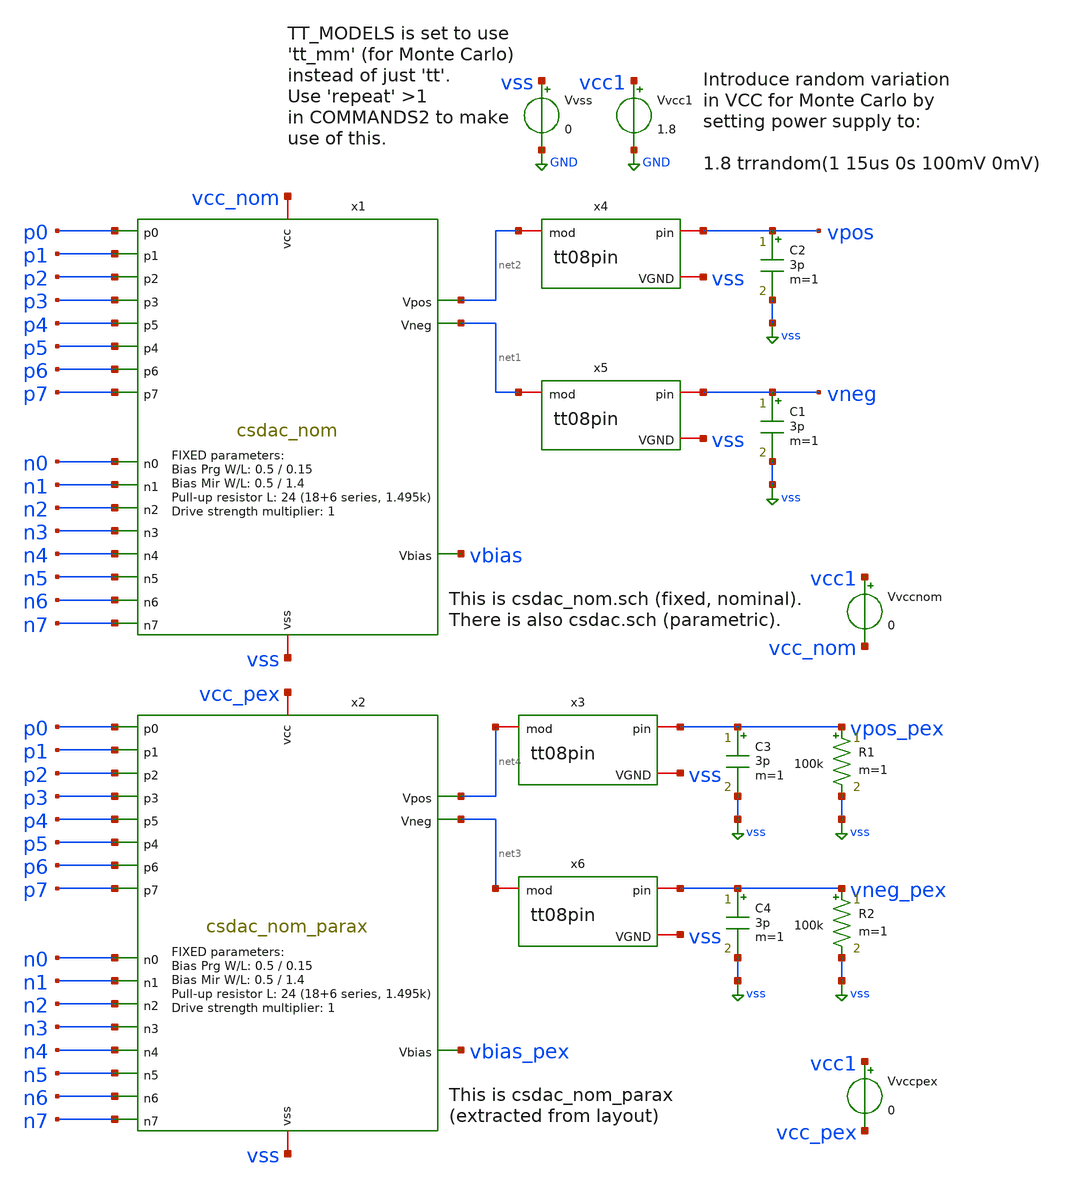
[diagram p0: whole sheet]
** sch_path: xschem/tb_csdac_nom.sch
**.subckt tb_csdac_nom
Vvcc1 vcc1 GND 1.8
Vvss vss GND 0
x1 vcc_nom vss p0 p1 p2 p3 p4 p5 p6 p7 n0 n1 n2 n3 n4 n5 n6 n7 net2 net1 vbias csdac_nom
x4 vpos net2 vss tt08pin
x5 vneg net1 vss tt08pin
C2 vpos vss 3p m=1
C1 vneg vss 3p m=1
x2 vcc_pex vss p0 p1 p2 p3 p4 p5 p6 p7 n0 n1 n2 n3 n4 n5 n6 n7 net4 net3 vbias_pex csdac_nom_parax
x3 vpos_pex net4 vss tt08pin
x6 vneg_pex net3 vss tt08pin
C3 vpos_pex vss 3p m=1
C4 vneg_pex vss 3p m=1
Vvccnom vcc1 vcc_nom 0
Vvccpex vcc1 vcc_pex 0
R1 vpos_pex vss 100k m=1
R2 vneg_pex vss 100k m=1
**** begin user architecture code



.param singlebits=0
.IF (singlebits == 1)
* Mode to just test each binary-weighted level:
Vxp0 p0 GND pulse 0v 1.8v 1u 1n 1n 1u 10u
Vxp1 p1 GND pulse 0v 1.8v 2u 1n 1n 1u 10u
Vxp2 p2 GND pulse 0v 1.8v 3u 1n 1n 1u 10u
Vxp3 p3 GND pulse 0v 1.8v 4u 1n 1n 1u 10u
Vxp4 p4 GND pulse 0v 1.8v 5u 1n 1n 1u 10u
Vxp5 p5 GND pulse 0v 1.8v 6u 1n 1n 1u 10u
Vxp6 p6 GND pulse 0v 1.8v 7u 1n 1n 1u 10u
Vxp7 p7 GND pulse 0v 1.8v 8u 1n 1n 1u 10u
Vxn0 n0 GND pulse 1.8v 0v 1u 1n 1n 1u 10u
Vxn1 n1 GND pulse 1.8v 0v 2u 1n 1n 1u 10u
Vxn2 n2 GND pulse 1.8v 0v 3u 1n 1n 1u 10u
Vxn3 n3 GND pulse 1.8v 0v 4u 1n 1n 1u 10u
Vxn4 n4 GND pulse 1.8v 0v 5u 1n 1n 1u 10u
Vxn5 n5 GND pulse 1.8v 0v 6u 1n 1n 1u 10u
Vxn6 n6 GND pulse 1.8v 0v 7u 1n 1n 1u 10u
Vxn7 n7 GND pulse 1.8v 0v 8u 1n 1n 1u 10u
.ELSEIF (singlebits == 0)
* Mode to test full 0..255 trange:
Vxp0 p0 GND pulse 1.8v 0v 0n 1n 1n 39n 80n
Vxp1 p1 GND pulse 1.8v 0v 0n 1n 1n 79n 160n
Vxp2 p2 GND pulse 1.8v 0v 0n 1n 1n 159n 320n
Vxp3 p3 GND pulse 1.8v 0v 0n 1n 1n 319n 640n
Vxp4 p4 GND pulse 1.8v 0v 0n 1n 1n 639n 1280n
Vxp5 p5 GND pulse 1.8v 0v 0n 1n 1n 1279n 2560n
Vxp6 p6 GND pulse 1.8v 0v 0n 1n 1n 2559n 5120n
Vxp7 p7 GND pulse 1.8v 0v 0n 1n 1n 5119n 10240n
Vxn0 n0 GND pulse 0v 1.8v 0n 1n 1n 39n 80n
Vxn1 n1 GND pulse 0v 1.8v 0n 1n 1n 79n 160n
Vxn2 n2 GND pulse 0v 1.8v 0n 1n 1n 159n 320n
Vxn3 n3 GND pulse 0v 1.8v 0n 1n 1n 319n 640n
Vxn4 n4 GND pulse 0v 1.8v 0n 1n 1n 639n 1280n
Vxn5 n5 GND pulse 0v 1.8v 0n 1n 1n 1279n 2560n
Vxn6 n6 GND pulse 0v 1.8v 0n 1n 1n 2559n 5120n
Vxn7 n7 GND pulse 0v 1.8v 0n 1n 1n 5119n 10240n
.ENDIF

.options savecurrents
.control

  * If using Monte Carlo, change to repeat to (say) 5:
  repeat 1
    save all
    tran 1n 12.8u
    write tb_csdac.raw i(vvss) vcc1
    + i(vvccnom) vpos     vneg     vbias
    + i(vvccpex) vpos_pex vneg_pex vbias_pex
    set appendwrite
    reset
  end

*  save all
*  *reset
*  *alterparam MPW=4
*  *alterparam MMW=4
*  tran 1n 12.8u
*  write 11.raw i(vvcc) i(vvss) vpos vneg vbias

*  set appendwrite
*  alterparam MPW=4
*  alterparam MMW=4
*  reset
*  tran 1n 12.8u
*  write 11.raw i(vvcc) i(vvss) vpos vneg vbias

.endc




** opencircuitdesign pdks install
.lib $::SKYWATER_MODELS/sky130.lib.spice tt


**** end user architecture code
**.ends

* expanding   symbol:  csdac_nom.sym # of pins=21
** sym_path: xschem/csdac_nom.sym
** sch_path: xschem/csdac_nom.sch
.subckt csdac_nom vcc vss p0 p1 p2 p3 p4 p5 p6 p7 n0 n1 n2 n3 n4 n5 n6 n7 Vpos Vneg Vbias
*.iopin vcc
*.iopin vss
*.ipin p0
*.ipin n0
*.ipin p1
*.ipin n1
*.ipin p2
*.ipin n2
*.ipin p3
*.ipin n3
*.ipin p4
*.ipin n4
*.ipin p5
*.ipin n5
*.ipin p6
*.ipin n6
*.ipin p7
*.ipin n7
*.opin Vpos
*.opin Vneg
*.opin Vbias
XMprog Vbias vss vcc vcc sky130_fd_pr__pfet_01v8 L=0.15 W=0.5 nf=1 ad='int((nf+1)/2) * W/nf * 0.29' as='int((nf+2)/2) * W/nf * 0.29'
+ pd='2*int((nf+1)/2) * (W/nf + 0.29)' ps='2*int((nf+2)/2) * (W/nf + 0.29)' nrd='0.29 / W' nrs='0.29 / W'
+ sa=0 sb=0 sd=0 mult=1 m=1
XMmirror Vbias Vbias vss vss sky130_fd_pr__nfet_01v8 L=0.5 W=0.5 nf=1 ad='int((nf+1)/2) * W/nf * 0.29'
+ as='int((nf+2)/2) * W/nf * 0.29' pd='2*int((nf+1)/2) * (W/nf + 0.29)' ps='2*int((nf+2)/2) * (W/nf + 0.29)'
+ nrd='0.29 / W' nrs='0.29 / W' sa=0 sb=0 sd=0 mult=1 m=1
XMB0 IS0 Vbias vss vss sky130_fd_pr__nfet_01v8 L=16 W=0.5 nf=1 ad='int((nf+1)/2) * W/nf * 0.29' as='int((nf+2)/2) * W/nf * 0.29'
+ pd='2*int((nf+1)/2) * (W/nf + 0.29)' ps='2*int((nf+2)/2) * (W/nf + 0.29)' nrd='0.29 / W' nrs='0.29 / W'
+ sa=0 sb=0 sd=0 mult=1 m=1
XMP0 Vpos p0 IS0 vss sky130_fd_pr__nfet_01v8 L=0.15 W=0.5 nf=1 ad='int((nf+1)/2) * W/nf * 0.29' as='int((nf+2)/2) * W/nf * 0.29'
+ pd='2*int((nf+1)/2) * (W/nf + 0.29)' ps='2*int((nf+2)/2) * (W/nf + 0.29)' nrd='0.29 / W' nrs='0.29 / W'
+ sa=0 sb=0 sd=0 mult=1 m=1
XMN0 Vneg n0 IS0 vss sky130_fd_pr__nfet_01v8 L=0.15 W=0.5 nf=1 ad='int((nf+1)/2) * W/nf * 0.29' as='int((nf+2)/2) * W/nf * 0.29'
+ pd='2*int((nf+1)/2) * (W/nf + 0.29)' ps='2*int((nf+2)/2) * (W/nf + 0.29)' nrd='0.29 / W' nrs='0.29 / W'
+ sa=0 sb=0 sd=0 mult=1 m=1
XMB1 IS1 Vbias vss vss sky130_fd_pr__nfet_01v8 L=8 W=0.5 nf=1 ad='int((nf+1)/2) * W/nf * 0.29' as='int((nf+2)/2) * W/nf * 0.29'
+ pd='2*int((nf+1)/2) * (W/nf + 0.29)' ps='2*int((nf+2)/2) * (W/nf + 0.29)' nrd='0.29 / W' nrs='0.29 / W'
+ sa=0 sb=0 sd=0 mult=1 m=1
XMP1 Vpos p1 IS1 vss sky130_fd_pr__nfet_01v8 L=0.15 W=0.5 nf=1 ad='int((nf+1)/2) * W/nf * 0.29' as='int((nf+2)/2) * W/nf * 0.29'
+ pd='2*int((nf+1)/2) * (W/nf + 0.29)' ps='2*int((nf+2)/2) * (W/nf + 0.29)' nrd='0.29 / W' nrs='0.29 / W'
+ sa=0 sb=0 sd=0 mult=1 m=1
XMN1 Vneg n1 IS1 vss sky130_fd_pr__nfet_01v8 L=0.15 W=0.5 nf=1 ad='int((nf+1)/2) * W/nf * 0.29' as='int((nf+2)/2) * W/nf * 0.29'
+ pd='2*int((nf+1)/2) * (W/nf + 0.29)' ps='2*int((nf+2)/2) * (W/nf + 0.29)' nrd='0.29 / W' nrs='0.29 / W'
+ sa=0 sb=0 sd=0 mult=1 m=1
XMB2 IS2 Vbias vss vss sky130_fd_pr__nfet_01v8 L=4 W=0.5 nf=1 ad='int((nf+1)/2) * W/nf * 0.29' as='int((nf+2)/2) * W/nf * 0.29'
+ pd='2*int((nf+1)/2) * (W/nf + 0.29)' ps='2*int((nf+2)/2) * (W/nf + 0.29)' nrd='0.29 / W' nrs='0.29 / W'
+ sa=0 sb=0 sd=0 mult=1 m=1
XMP2 Vpos p2 IS2 vss sky130_fd_pr__nfet_01v8 L=0.15 W=0.5 nf=1 ad='int((nf+1)/2) * W/nf * 0.29' as='int((nf+2)/2) * W/nf * 0.29'
+ pd='2*int((nf+1)/2) * (W/nf + 0.29)' ps='2*int((nf+2)/2) * (W/nf + 0.29)' nrd='0.29 / W' nrs='0.29 / W'
+ sa=0 sb=0 sd=0 mult=1 m=1
XMN2 Vneg n2 IS2 vss sky130_fd_pr__nfet_01v8 L=0.15 W=0.5 nf=1 ad='int((nf+1)/2) * W/nf * 0.29' as='int((nf+2)/2) * W/nf * 0.29'
+ pd='2*int((nf+1)/2) * (W/nf + 0.29)' ps='2*int((nf+2)/2) * (W/nf + 0.29)' nrd='0.29 / W' nrs='0.29 / W'
+ sa=0 sb=0 sd=0 mult=1 m=1
XMB3 IS3 Vbias vss vss sky130_fd_pr__nfet_01v8 L=2.1 W=0.5 nf=1 ad='int((nf+1)/2) * W/nf * 0.29' as='int((nf+2)/2) * W/nf * 0.29'
+ pd='2*int((nf+1)/2) * (W/nf + 0.29)' ps='2*int((nf+2)/2) * (W/nf + 0.29)' nrd='0.29 / W' nrs='0.29 / W'
+ sa=0 sb=0 sd=0 mult=1 m=1
XMP3 Vpos p3 IS3 vss sky130_fd_pr__nfet_01v8 L=0.15 W=0.5 nf=1 ad='int((nf+1)/2) * W/nf * 0.29' as='int((nf+2)/2) * W/nf * 0.29'
+ pd='2*int((nf+1)/2) * (W/nf + 0.29)' ps='2*int((nf+2)/2) * (W/nf + 0.29)' nrd='0.29 / W' nrs='0.29 / W'
+ sa=0 sb=0 sd=0 mult=1 m=1
XMN3 Vneg n3 IS3 vss sky130_fd_pr__nfet_01v8 L=0.15 W=0.5 nf=1 ad='int((nf+1)/2) * W/nf * 0.29' as='int((nf+2)/2) * W/nf * 0.29'
+ pd='2*int((nf+1)/2) * (W/nf + 0.29)' ps='2*int((nf+2)/2) * (W/nf + 0.29)' nrd='0.29 / W' nrs='0.29 / W'
+ sa=0 sb=0 sd=0 mult=1 m=1
XMB4 IS4 Vbias vss vss sky130_fd_pr__nfet_01v8 L=1 W=0.5 nf=1 ad='int((nf+1)/2) * W/nf * 0.29' as='int((nf+2)/2) * W/nf * 0.29'
+ pd='2*int((nf+1)/2) * (W/nf + 0.29)' ps='2*int((nf+2)/2) * (W/nf + 0.29)' nrd='0.29 / W' nrs='0.29 / W'
+ sa=0 sb=0 sd=0 mult=1 m=1
XMP4 Vpos p4 IS4 vss sky130_fd_pr__nfet_01v8 L=0.15 W=0.5 nf=1 ad='int((nf+1)/2) * W/nf * 0.29' as='int((nf+2)/2) * W/nf * 0.29'
+ pd='2*int((nf+1)/2) * (W/nf + 0.29)' ps='2*int((nf+2)/2) * (W/nf + 0.29)' nrd='0.29 / W' nrs='0.29 / W'
+ sa=0 sb=0 sd=0 mult=1 m=1
XMN4 Vneg n4 IS4 vss sky130_fd_pr__nfet_01v8 L=0.15 W=0.5 nf=1 ad='int((nf+1)/2) * W/nf * 0.29' as='int((nf+2)/2) * W/nf * 0.29'
+ pd='2*int((nf+1)/2) * (W/nf + 0.29)' ps='2*int((nf+2)/2) * (W/nf + 0.29)' nrd='0.29 / W' nrs='0.29 / W'
+ sa=0 sb=0 sd=0 mult=1 m=1
XMB5 IS5 Vbias vss vss sky130_fd_pr__nfet_01v8 L=2.3 W=1.9 nf=1 ad='int((nf+1)/2) * W/nf * 0.29' as='int((nf+2)/2) * W/nf * 0.29'
+ pd='2*int((nf+1)/2) * (W/nf + 0.29)' ps='2*int((nf+2)/2) * (W/nf + 0.29)' nrd='0.29 / W' nrs='0.29 / W'
+ sa=0 sb=0 sd=0 mult=1 m=1
XMP5 Vpos p5 IS5 vss sky130_fd_pr__nfet_01v8 L=0.15 W=1 nf=1 ad='int((nf+1)/2) * W/nf * 0.29' as='int((nf+2)/2) * W/nf * 0.29'
+ pd='2*int((nf+1)/2) * (W/nf + 0.29)' ps='2*int((nf+2)/2) * (W/nf + 0.29)' nrd='0.29 / W' nrs='0.29 / W'
+ sa=0 sb=0 sd=0 mult=1 m=1
XMN5 Vneg n5 IS5 vss sky130_fd_pr__nfet_01v8 L=0.15 W=1 nf=1 ad='int((nf+1)/2) * W/nf * 0.29' as='int((nf+2)/2) * W/nf * 0.29'
+ pd='2*int((nf+1)/2) * (W/nf + 0.29)' ps='2*int((nf+2)/2) * (W/nf + 0.29)' nrd='0.29 / W' nrs='0.29 / W'
+ sa=0 sb=0 sd=0 mult=1 m=1
XMB6 IS6 Vbias vss vss sky130_fd_pr__nfet_01v8 L=0.5 W=1.1 nf=1 ad='int((nf+1)/2) * W/nf * 0.29' as='int((nf+2)/2) * W/nf * 0.29'
+ pd='2*int((nf+1)/2) * (W/nf + 0.29)' ps='2*int((nf+2)/2) * (W/nf + 0.29)' nrd='0.29 / W' nrs='0.29 / W'
+ sa=0 sb=0 sd=0 mult=1 m=1
XMP6 Vpos p6 IS6 vss sky130_fd_pr__nfet_01v8 L=0.15 W=2 nf=1 ad='int((nf+1)/2) * W/nf * 0.29' as='int((nf+2)/2) * W/nf * 0.29'
+ pd='2*int((nf+1)/2) * (W/nf + 0.29)' ps='2*int((nf+2)/2) * (W/nf + 0.29)' nrd='0.29 / W' nrs='0.29 / W'
+ sa=0 sb=0 sd=0 mult=1 m=1
XMN6 Vneg n6 IS6 vss sky130_fd_pr__nfet_01v8 L=0.15 W=2 nf=1 ad='int((nf+1)/2) * W/nf * 0.29' as='int((nf+2)/2) * W/nf * 0.29'
+ pd='2*int((nf+1)/2) * (W/nf + 0.29)' ps='2*int((nf+2)/2) * (W/nf + 0.29)' nrd='0.29 / W' nrs='0.29 / W'
+ sa=0 sb=0 sd=0 mult=1 m=1
XMB7 IS7 Vbias vss vss sky130_fd_pr__nfet_01v8 L=0.5 W=2.1 nf=1 ad='int((nf+1)/2) * W/nf * 0.29' as='int((nf+2)/2) * W/nf * 0.29'
+ pd='2*int((nf+1)/2) * (W/nf + 0.29)' ps='2*int((nf+2)/2) * (W/nf + 0.29)' nrd='0.29 / W' nrs='0.29 / W'
+ sa=0 sb=0 sd=0 mult=1 m=1
XMP7 Vpos p7 IS7 vss sky130_fd_pr__nfet_01v8 L=0.15 W=3 nf=1 ad='int((nf+1)/2) * W/nf * 0.29' as='int((nf+2)/2) * W/nf * 0.29'
+ pd='2*int((nf+1)/2) * (W/nf + 0.29)' ps='2*int((nf+2)/2) * (W/nf + 0.29)' nrd='0.29 / W' nrs='0.29 / W'
+ sa=0 sb=0 sd=0 mult=1 m=1
XMN7 Vneg n7 IS7 vss sky130_fd_pr__nfet_01v8 L=0.15 W=3 nf=1 ad='int((nf+1)/2) * W/nf * 0.29' as='int((nf+2)/2) * W/nf * 0.29'
+ pd='2*int((nf+1)/2) * (W/nf + 0.29)' ps='2*int((nf+2)/2) * (W/nf + 0.29)' nrd='0.29 / W' nrs='0.29 / W'
+ sa=0 sb=0 sd=0 mult=1 m=1
XRLP Vpos net1 vss sky130_fd_pr__res_high_po_5p73 L=28 mult=1 m=1
XRLN Vneg net2 vss sky130_fd_pr__res_high_po_5p73 L=28 mult=1 m=1
XRSP net1 vcc vss sky130_fd_pr__res_high_po_5p73 L=11 mult=1 m=1
XRSN net2 vcc vss sky130_fd_pr__res_high_po_5p73 L=11 mult=1 m=1
.ends


* expanding   symbol:  tt08pin.sym # of pins=3
** sym_path: xschem/tt08pin.sym
** sch_path: xschem/tt08pin.sch
.subckt tt08pin pin mod VGND
*.iopin pin
*.iopin VGND
*.iopin mod
R1 net1 pin 1 m=1
C1 pin VGND 1p m=1
L1 net2 net1 1n m=1
V1 VAPWR VGND 3.3
C2 net2 VGND 2p m=1
R2 net3 net2 50 m=1
XM2 net3 VGND mod VAPWR sky130_fd_pr__pfet_g5v0d10v5 L=0.5 W=100 nf=20 ad='int((nf+1)/2) * W/nf * 0.29'
+ as='int((nf+2)/2) * W/nf * 0.29' pd='2*int((nf+1)/2) * (W/nf + 0.29)' ps='2*int((nf+2)/2) * (W/nf + 0.29)'
+ nrd='0.29 / W' nrs='0.29 / W' sa=0 sb=0 sd=0 mult=1 m=1
XM1 net3 VAPWR mod VGND sky130_fd_pr__nfet_g5v0d10v5 L=0.5 W=60 nf=12 ad='int((nf+1)/2) * W/nf * 0.29'
+ as='int((nf+2)/2) * W/nf * 0.29' pd='2*int((nf+1)/2) * (W/nf + 0.29)' ps='2*int((nf+2)/2) * (W/nf + 0.29)'
+ nrd='0.29 / W' nrs='0.29 / W' sa=0 sb=0 sd=0 mult=1 m=1
XM4 net3 VAPWR VGND VAPWR sky130_fd_pr__pfet_g5v0d10v5 L=0.5 W=100 nf=20 ad='int((nf+1)/2) * W/nf * 0.29'
+ as='int((nf+2)/2) * W/nf * 0.29' pd='2*int((nf+1)/2) * (W/nf + 0.29)' ps='2*int((nf+2)/2) * (W/nf + 0.29)'
+ nrd='0.29 / W' nrs='0.29 / W' sa=0 sb=0 sd=0 mult=15 m=15
XM3 net3 VGND VGND VGND sky130_fd_pr__nfet_g5v0d10v5 L=0.5 W=60 nf=12 ad='int((nf+1)/2) * W/nf * 0.29'
+ as='int((nf+2)/2) * W/nf * 0.29' pd='2*int((nf+1)/2) * (W/nf + 0.29)' ps='2*int((nf+2)/2) * (W/nf + 0.29)'
+ nrd='0.29 / W' nrs='0.29 / W' sa=0 sb=0 sd=0 mult=15 m=15
C3 mod VGND 250f m=1
.ends


* expanding   symbol:  csdac_nom_parax.sym # of pins=21
** sym_path: xschem/csdac_nom.sym
.include [file normalize ../mag/csdac_nom.sim.spice]
.GLOBAL GND
.GLOBAL vss
.GLOBAL VGND
.GLOBAL VAPWR
.end
